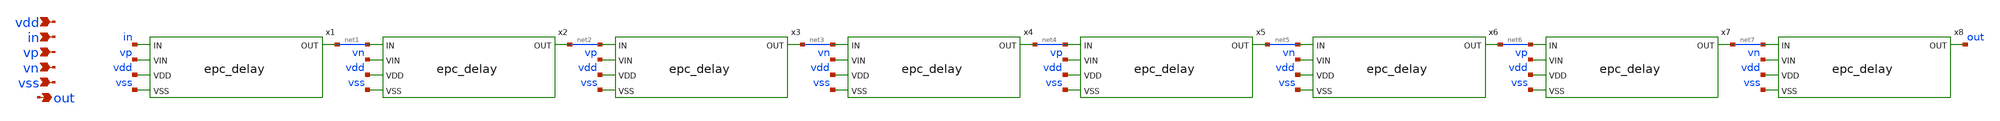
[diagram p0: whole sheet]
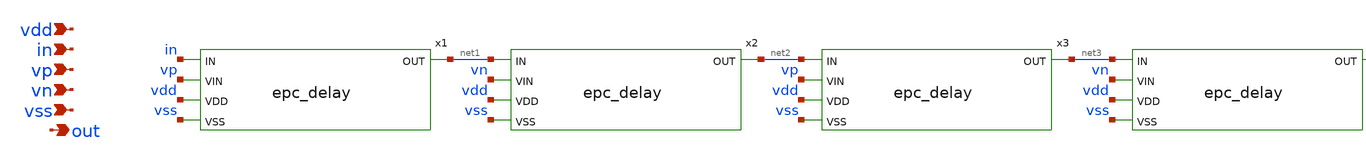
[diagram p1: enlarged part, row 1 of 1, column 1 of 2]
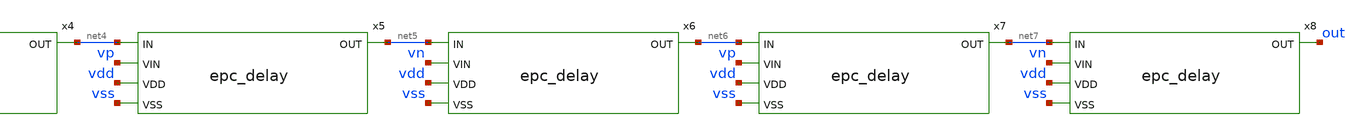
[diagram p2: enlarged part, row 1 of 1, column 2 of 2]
** sch_path: xschem/epc_delay_line.sch
**.subckt epc_delay_line vdd in vp vn vss out
*.ipin vdd
*.ipin in
*.ipin vp
*.ipin vn
*.ipin vss
*.opin out
x1 in net1 vp vdd vss epc_delay
x2 net1 net2 vn vdd vss epc_delay
x3 net2 net3 vp vdd vss epc_delay
x4 net3 net4 vn vdd vss epc_delay
x5 net4 net5 vp vdd vss epc_delay
x6 net5 net6 vn vdd vss epc_delay
x7 net6 net7 vp vdd vss epc_delay
x8 net7 out vn vdd vss epc_delay
**.ends

* expanding   symbol:  epc_delay.sym # of pins=5
** sym_path: xschem/epc_delay.sym
** sch_path: xschem/epc_delay.sch
.subckt epc_delay IN OUT VIN VDD VSS
*.ipin VDD
*.ipin VIN
*.ipin IN
*.ipin VSS
*.opin OUT
.param W_N=0.5 L_N=0.5 W_P=1.0 L_P=0.5
XM1 net2 VIN VDD VDD sky130_fd_pr__pfet_01v8_lvt L=L_P W=W_P nf=1 ad='int((nf+1)/2) * W/nf * 0.29' as='int((nf+2)/2) * W/nf * 0.29'
+ pd='2*int((nf+1)/2) * (W/nf + 0.29)' ps='2*int((nf+2)/2) * (W/nf + 0.29)' nrd='0.29 / W' nrs='0.29 / W'
+ sa=0 sb=0 sd=0 mult=1 m=1
XM2 OUT IN net2 VDD sky130_fd_pr__pfet_01v8_lvt L=L_P W=W_P nf=1 ad='int((nf+1)/2) * W/nf * 0.29' as='int((nf+2)/2) * W/nf * 0.29'
+ pd='2*int((nf+1)/2) * (W/nf + 0.29)' ps='2*int((nf+2)/2) * (W/nf + 0.29)' nrd='0.29 / W' nrs='0.29 / W'
+ sa=0 sb=0 sd=0 mult=1 m=1
XM3 OUT IN net1 VSS sky130_fd_pr__nfet_01v8_lvt L=L_N W=W_N nf=1 ad='int((nf+1)/2) * W/nf * 0.29' as='int((nf+2)/2) * W/nf * 0.29'
+ pd='2*int((nf+1)/2) * (W/nf + 0.29)' ps='2*int((nf+2)/2) * (W/nf + 0.29)' nrd='0.29 / W' nrs='0.29 / W'
+ sa=0 sb=0 sd=0 mult=1 m=1
XM4 net1 VIN VSS VSS sky130_fd_pr__nfet_01v8_lvt L=L_N W=W_N nf=1 ad='int((nf+1)/2) * W/nf * 0.29' as='int((nf+2)/2) * W/nf * 0.29'
+ pd='2*int((nf+1)/2) * (W/nf + 0.29)' ps='2*int((nf+2)/2) * (W/nf + 0.29)' nrd='0.29 / W' nrs='0.29 / W'
+ sa=0 sb=0 sd=0 mult=1 m=1
.ends

.end
